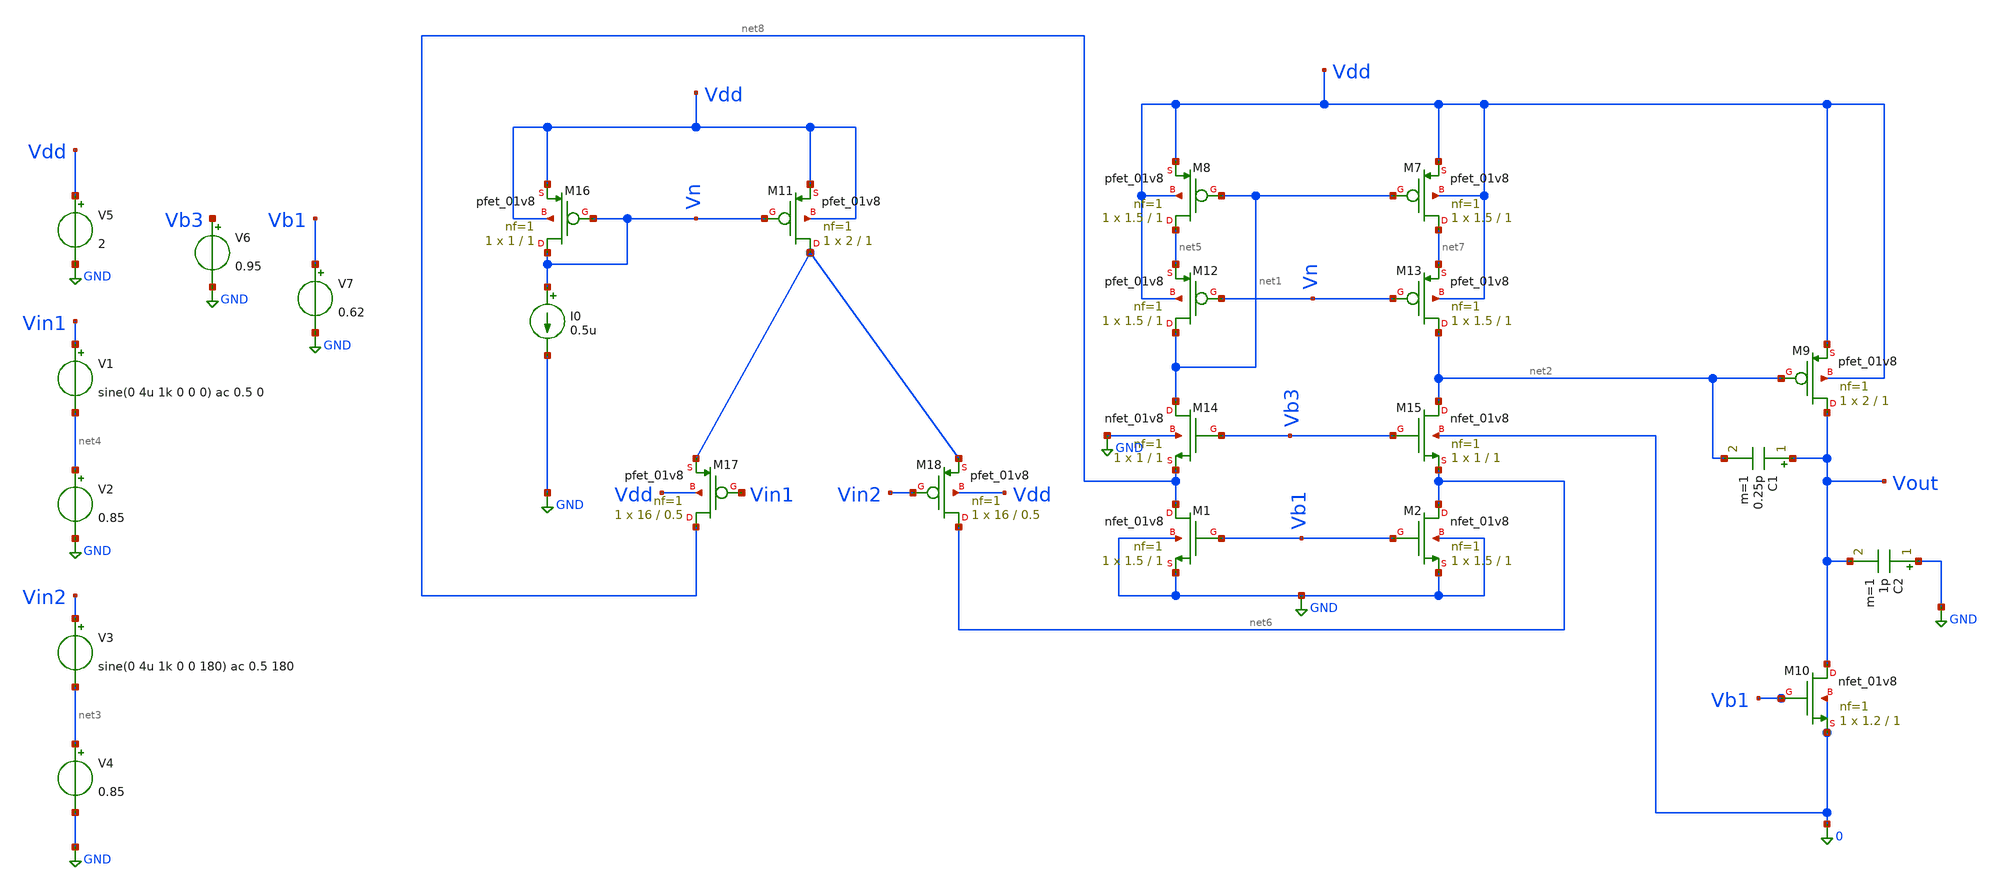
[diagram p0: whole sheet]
** sch_path: dac2.sch
**.subckt dac2
XM1 net8 Vb1 GND GND sky130_fd_pr__nfet_01v8 L=1 W=1.5 nf=1 ad='int((nf+1)/2) * W/nf * 0.29' as='int((nf+2)/2) * W/nf * 0.29'
+ pd='2*int((nf+1)/2) * (W/nf + 0.29)' ps='2*int((nf+2)/2) * (W/nf + 0.29)' nrd='0.29 / W' nrs='0.29 / W'
+ sa=0 sb=0 sd=0 mult=1 m=1
XM2 net6 Vb1 GND GND sky130_fd_pr__nfet_01v8 L=1 W=1.5 nf=1 ad='int((nf+1)/2) * W/nf * 0.29' as='int((nf+2)/2) * W/nf * 0.29'
+ pd='2*int((nf+1)/2) * (W/nf + 0.29)' ps='2*int((nf+2)/2) * (W/nf + 0.29)' nrd='0.29 / W' nrs='0.29 / W'
+ sa=0 sb=0 sd=0 mult=1 m=1
XM7 net7 net1 Vdd Vdd sky130_fd_pr__pfet_01v8 L=1 W=1.5 nf=1 ad='int((nf+1)/2) * W/nf * 0.29' as='int((nf+2)/2) * W/nf * 0.29'
+ pd='2*int((nf+1)/2) * (W/nf + 0.29)' ps='2*int((nf+2)/2) * (W/nf + 0.29)' nrd='0.29 / W' nrs='0.29 / W'
+ sa=0 sb=0 sd=0 mult=1 m=1
XM8 net5 net1 Vdd Vdd sky130_fd_pr__pfet_01v8 L=1 W=1.5 nf=1 ad='int((nf+1)/2) * W/nf * 0.29' as='int((nf+2)/2) * W/nf * 0.29'
+ pd='2*int((nf+1)/2) * (W/nf + 0.29)' ps='2*int((nf+2)/2) * (W/nf + 0.29)' nrd='0.29 / W' nrs='0.29 / W'
+ sa=0 sb=0 sd=0 mult=1 m=1
I0 Vn GND 0.5u
XM9 Vout net2 Vdd Vdd sky130_fd_pr__pfet_01v8 L=1 W=2 nf=1 ad='int((nf+1)/2) * W/nf * 0.29' as='int((nf+2)/2) * W/nf * 0.29'
+ pd='2*int((nf+1)/2) * (W/nf + 0.29)' ps='2*int((nf+2)/2) * (W/nf + 0.29)' nrd='0.29 / W' nrs='0.29 / W'
+ sa=0 sb=0 sd=0 mult=1 m=1
XM10 Vout Vb1 0 0 sky130_fd_pr__nfet_01v8 L=1 W=1.2 nf=1 ad='int((nf+1)/2) * W/nf * 0.29' as='int((nf+2)/2) * W/nf * 0.29'
+ pd='2*int((nf+1)/2) * (W/nf + 0.29)' ps='2*int((nf+2)/2) * (W/nf + 0.29)' nrd='0.29 / W' nrs='0.29 / W'
+ sa=0 sb=0 sd=0 mult=1 m=1
C1 Vout net2 0.25p m=1
C2 GND Vout 1p m=1
V1 Vin1 net4 sine(0 4u 1k 0 0 0) ac 0.5 0
V2 net4 GND 0.85
V3 Vin2 net3 sine(0 4u 1k 0 0 180) ac 0.5 180
V4 net3 GND 0.85
V5 Vdd GND 2
XM12 net1 Vn net5 Vdd sky130_fd_pr__pfet_01v8 L=1 W=1.5 nf=1 ad='int((nf+1)/2) * W/nf * 0.29' as='int((nf+2)/2) * W/nf * 0.29'
+ pd='2*int((nf+1)/2) * (W/nf + 0.29)' ps='2*int((nf+2)/2) * (W/nf + 0.29)' nrd='0.29 / W' nrs='0.29 / W'
+ sa=0 sb=0 sd=0 mult=1 m=1
XM13 net2 Vn net7 Vdd sky130_fd_pr__pfet_01v8 L=1 W=1.5 nf=1 ad='int((nf+1)/2) * W/nf * 0.29' as='int((nf+2)/2) * W/nf * 0.29'
+ pd='2*int((nf+1)/2) * (W/nf + 0.29)' ps='2*int((nf+2)/2) * (W/nf + 0.29)' nrd='0.29 / W' nrs='0.29 / W'
+ sa=0 sb=0 sd=0 mult=1 m=1
XM14 net1 Vb3 net8 GND sky130_fd_pr__nfet_01v8 L=1 W=1 nf=1 ad='int((nf+1)/2) * W/nf * 0.29' as='int((nf+2)/2) * W/nf * 0.29'
+ pd='2*int((nf+1)/2) * (W/nf + 0.29)' ps='2*int((nf+2)/2) * (W/nf + 0.29)' nrd='0.29 / W' nrs='0.29 / W'
+ sa=0 sb=0 sd=0 mult=1 m=1
XM15 net2 Vb3 net6 0 sky130_fd_pr__nfet_01v8 L=1 W=1 nf=1 ad='int((nf+1)/2) * W/nf * 0.29' as='int((nf+2)/2) * W/nf * 0.29'
+ pd='2*int((nf+1)/2) * (W/nf + 0.29)' ps='2*int((nf+2)/2) * (W/nf + 0.29)' nrd='0.29 / W' nrs='0.29 / W'
+ sa=0 sb=0 sd=0 mult=1 m=1
V6 Vb3 GND 0.95
XM11 net9 Vn Vdd Vdd sky130_fd_pr__pfet_01v8 L=1 W=2 nf=1 ad='int((nf+1)/2) * W/nf * 0.29' as='int((nf+2)/2) * W/nf * 0.29'
+ pd='2*int((nf+1)/2) * (W/nf + 0.29)' ps='2*int((nf+2)/2) * (W/nf + 0.29)' nrd='0.29 / W' nrs='0.29 / W'
+ sa=0 sb=0 sd=0 mult=1 m=1
XM16 Vn Vn Vdd Vdd sky130_fd_pr__pfet_01v8 L=1 W=1 nf=1 ad='int((nf+1)/2) * W/nf * 0.29' as='int((nf+2)/2) * W/nf * 0.29'
+ pd='2*int((nf+1)/2) * (W/nf + 0.29)' ps='2*int((nf+2)/2) * (W/nf + 0.29)' nrd='0.29 / W' nrs='0.29 / W'
+ sa=0 sb=0 sd=0 mult=1 m=1
XM17 net8 Vin1 net9 Vdd sky130_fd_pr__pfet_01v8 L=0.5 W=16 nf=1 ad='int((nf+1)/2) * W/nf * 0.29' as='int((nf+2)/2) * W/nf * 0.29'
+ pd='2*int((nf+1)/2) * (W/nf + 0.29)' ps='2*int((nf+2)/2) * (W/nf + 0.29)' nrd='0.29 / W' nrs='0.29 / W'
+ sa=0 sb=0 sd=0 mult=1 m=1
XM18 net6 Vin2 net9 Vdd sky130_fd_pr__pfet_01v8 L=0.5 W=16 nf=1 ad='int((nf+1)/2) * W/nf * 0.29' as='int((nf+2)/2) * W/nf * 0.29'
+ pd='2*int((nf+1)/2) * (W/nf + 0.29)' ps='2*int((nf+2)/2) * (W/nf + 0.29)' nrd='0.29 / W' nrs='0.29 / W'
+ sa=0 sb=0 sd=0 mult=1 m=1
V7 Vb1 GND 0.62
**** begin user architecture code


.ac dec 10 1 10G
.tran 10u 5m

# Parameter-aware Subcircuit wrapper for NFET
.subckt sky130_fd_pr__nfet_01v8 d g s b w=1 l=0.15 nf=1 mult=1 ad=0 as=0 pd=0 ps=0 nrd=0 nrs=0 sa=0
+ sb=0 sd=0
.model ideal_n nmos vto=0.7 kp=160e-6
m1 d g s b ideal_n w={w} l={l}
.ends

# Parameter-aware Subcircuit wrapper for PFET
.subckt sky130_fd_pr__pfet_01v8 d g s b w=1 l=0.15 nf=1 mult=1 ad=0 as=0 pd=0 ps=0 nrd=0 nrs=0 sa=0
+ sb=0 sd=0
.model ideal_p pmos vto=-0.7 kp=45e-6
m1 d g s b ideal_p w={w} l={l}
.ends

.control
  run
  set color0=white
  set color1=black

  ; --- 1. Plot Transient Waveform ---
  setplot tran1
  plot v(Vin1) v(Vout)

  ; --- 2. Plot AC Bode Response (Gain & Phase) ---
  setplot ac1
  let phase_deg = (180/PI) * cph(v(Vout))
  let gain_db = db(v(Vout))
  plot gain_db phase_deg ylimit -60 100

  ; --- 3. Measure Bandwidth & Phase Margin in Console ---
  meas ac gbw when gain_db=0
  meas ac phase_at_gbw find phase_deg when gain_db=0
  let phase_margin = 180 + phase_at_gbw
  print gbw phase_margin
.endc


**** end user architecture code
**.ends
.GLOBAL GND
.end
